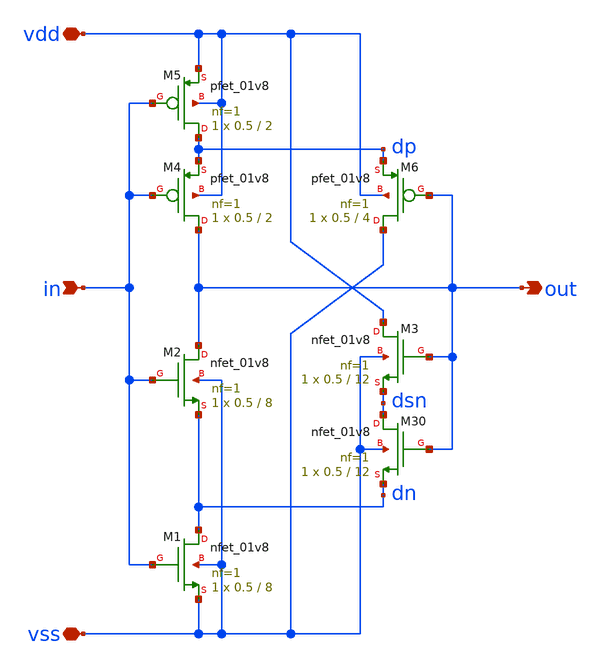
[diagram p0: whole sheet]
** sch_path: xschem/schmittinv.sch
* Copyright 2020 Stefan Frederik Schippers
* Licensed under the Apache License, Version 2.0 (the "License");
* you may not use this file except in compliance with the License.
* You may obtain a copy of the License at
* https://www.apache.org/licenses/LICENSE-2.0
* Unless required by applicable law or agreed to in writing, software
* distributed under the License is distributed on an "AS IS" BASIS,
* WITHOUT WARRANTIES OR CONDITIONS OF ANY KIND, either express or implied.
* See the License for the specific language governing permissions and
* limitations under the License.
**.subckt schmittinv vdd vss in out
*.iopin vdd
*.iopin vss
*.ipin in
*.opin out
XM1 dn in vss vss sky130_fd_pr__nfet_01v8 L=8 W=0.5 nf=1 ad='int((1 + 1)/2) * 0.5 / 1 * 0.29' as='int((1 + 2)/2) * 0.5 / 1 * 0.29'
+ pd='2*int((1 + 1)/2) * (0.5 / 1 + 0.29)' ps='2*int((1 + 2)/2) * (0.5 / 1 + 0.29)' nrd='0.29 / 0.5 ' nrs='0.29 / 0.5 '
+ sa=0 sb=0 sd=0 mult=1 m=1
XM5 dp in vdd vdd sky130_fd_pr__pfet_01v8 L=2 W=0.5 nf=1 ad='int((nf+1)/2) * W/nf * 0.29' as='int((nf+2)/2) * W/nf * 0.29'
+ pd='2*int((nf+1)/2) * (W/nf + 0.29)' ps='2*int((nf+2)/2) * (W/nf + 0.29)' nrd='0.29 / W' nrs='0.29 / W'
+ sa=0 sb=0 sd=0 mult=1 m=1
XM3 vdd out dsn vss sky130_fd_pr__nfet_01v8 L=12 W=0.5 nf=1 ad='int((1 + 1)/2) * 0.5 / 1 * 0.29' as='int((1 + 2)/2) * 0.5 / 1 * 0.29'
+ pd='2*int((1 + 1)/2) * (0.5 / 1 + 0.29)' ps='2*int((1 + 2)/2) * (0.5 / 1 + 0.29)' nrd='0.29 / 0.5 ' nrs='0.29 / 0.5 '
+ sa=0 sb=0 sd=0 mult=1 m=1
XM6 vss out dp vdd sky130_fd_pr__pfet_01v8 L=4 W=0.5 nf=1 ad='int((nf+1)/2) * W/nf * 0.29' as='int((nf+2)/2) * W/nf * 0.29'
+ pd='2*int((nf+1)/2) * (W/nf + 0.29)' ps='2*int((nf+2)/2) * (W/nf + 0.29)' nrd='0.29 / W' nrs='0.29 / W'
+ sa=0 sb=0 sd=0 mult=1 m=1
XM4 out in dp vdd sky130_fd_pr__pfet_01v8 L=2 W=0.5 nf=1 ad='int((nf+1)/2) * W/nf * 0.29' as='int((nf+2)/2) * W/nf * 0.29'
+ pd='2*int((nf+1)/2) * (W/nf + 0.29)' ps='2*int((nf+2)/2) * (W/nf + 0.29)' nrd='0.29 / W' nrs='0.29 / W'
+ sa=0 sb=0 sd=0 mult=1 m=1
XM2 out in dn vss sky130_fd_pr__nfet_01v8 L=8 W=0.5 nf=1 ad='int((1 + 1)/2) * 0.5 / 1 * 0.29' as='int((1 + 2)/2) * 0.5 / 1 * 0.29'
+ pd='2*int((1 + 1)/2) * (0.5 / 1 + 0.29)' ps='2*int((1 + 2)/2) * (0.5 / 1 + 0.29)' nrd='0.29 / 0.5 ' nrs='0.29 / 0.5 '
+ sa=0 sb=0 sd=0 mult=1 m=1
XM30 dsn out dn vss sky130_fd_pr__nfet_01v8 L=12 W=0.5 nf=1 ad='int((1 + 1)/2) * 0.5 / 1 * 0.29' as='int((1 + 2)/2) * 0.5 / 1 * 0.29'
+ pd='2*int((1 + 1)/2) * (0.5 / 1 + 0.29)' ps='2*int((1 + 2)/2) * (0.5 / 1 + 0.29)' nrd='0.29 / 0.5 ' nrs='0.29 / 0.5 '
+ sa=0 sb=0 sd=0 mult=1 m=1
**.ends
.end
